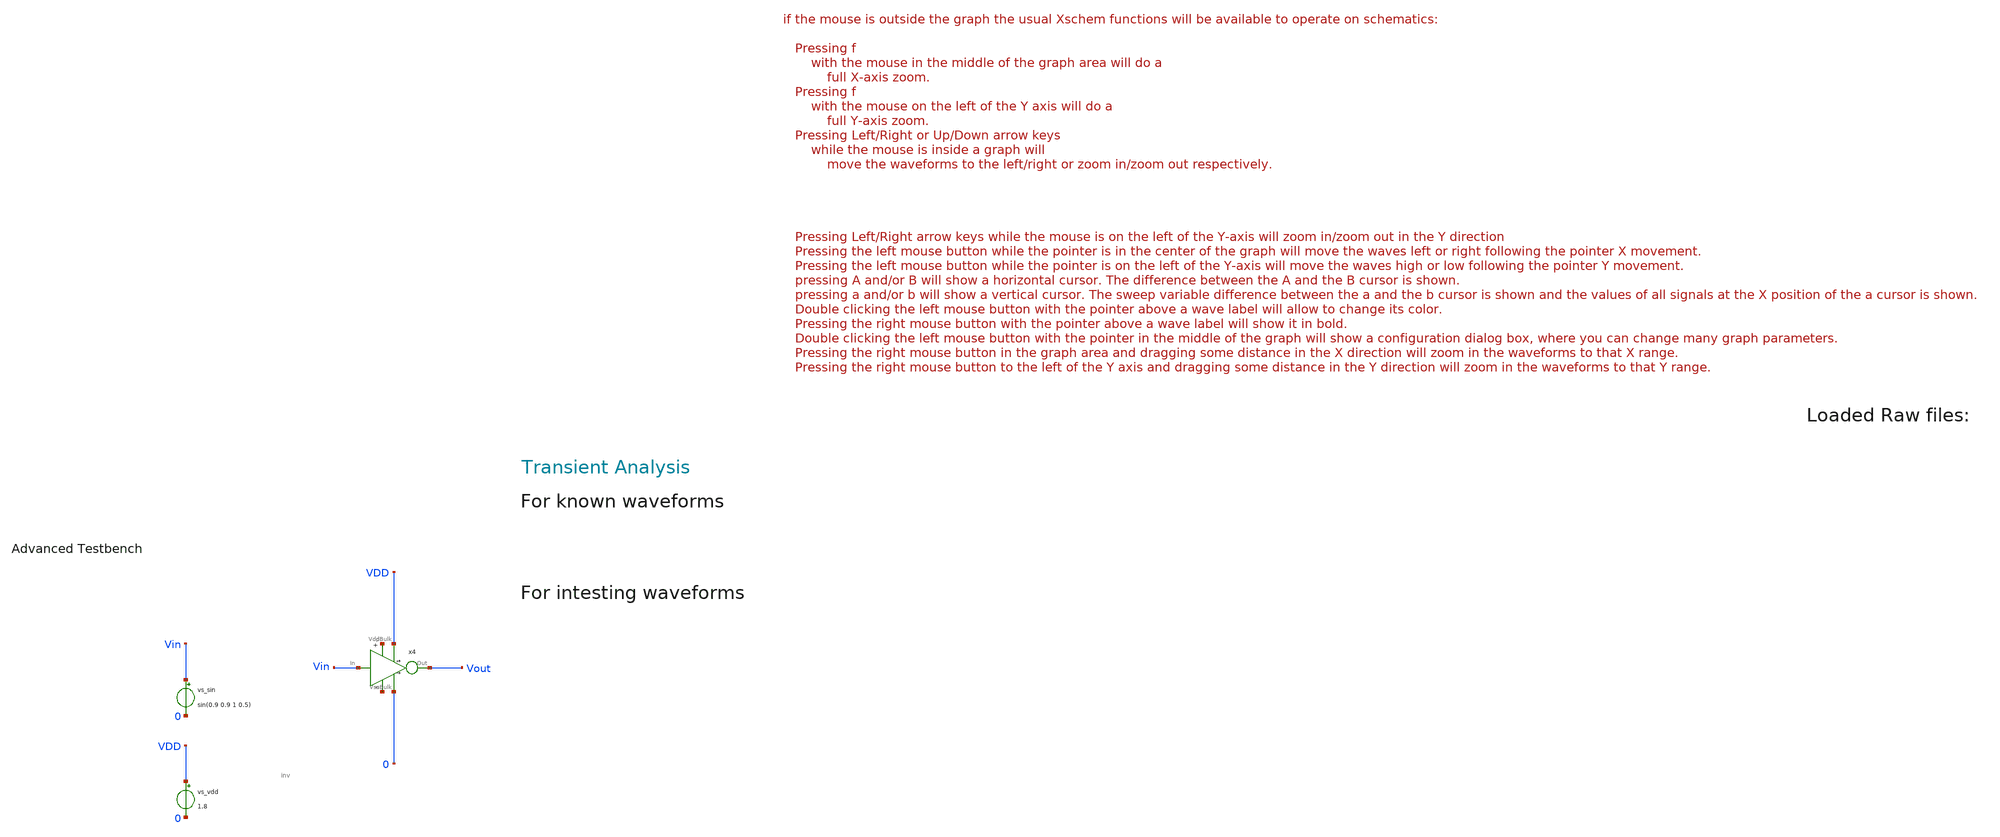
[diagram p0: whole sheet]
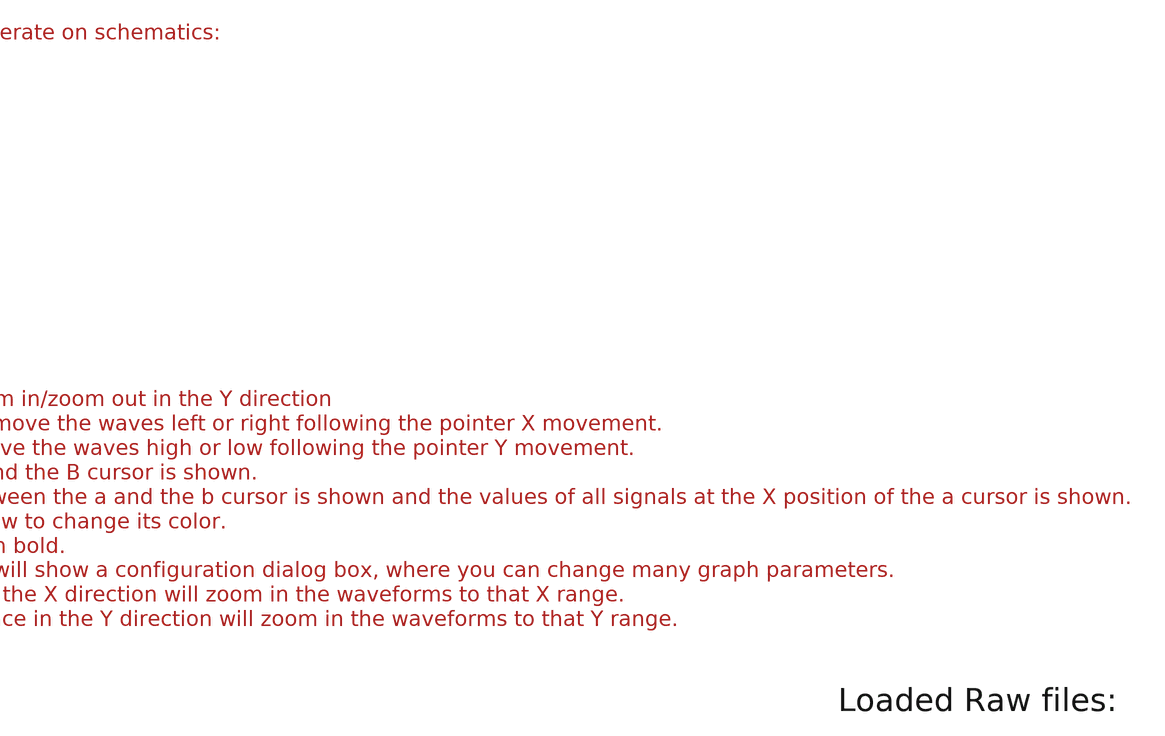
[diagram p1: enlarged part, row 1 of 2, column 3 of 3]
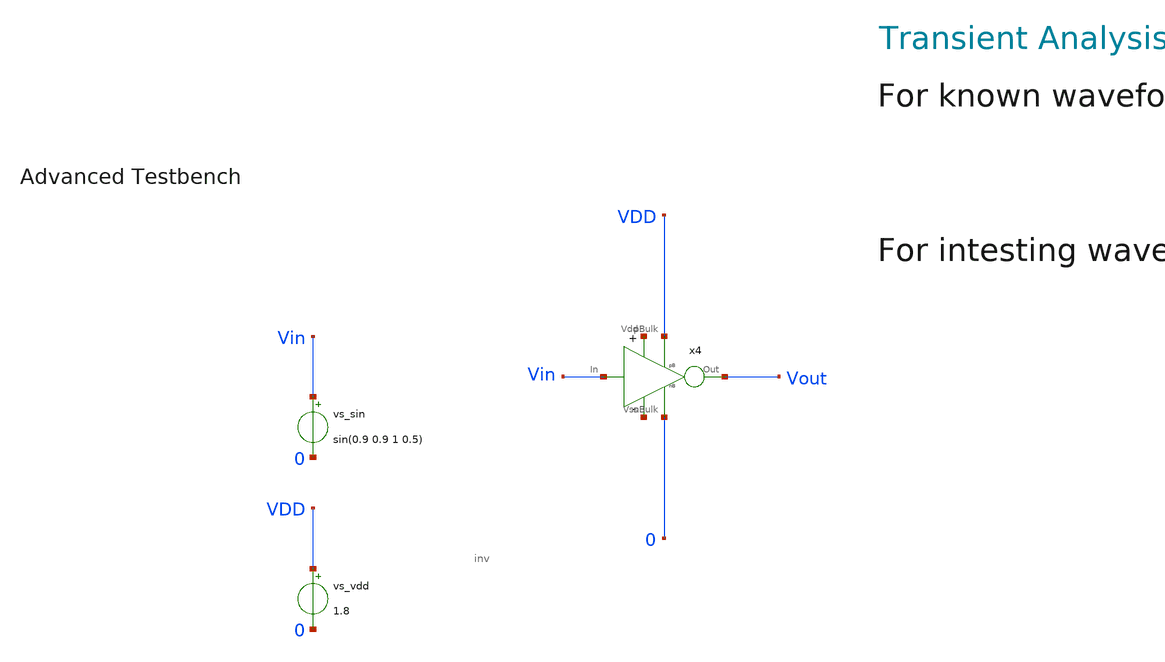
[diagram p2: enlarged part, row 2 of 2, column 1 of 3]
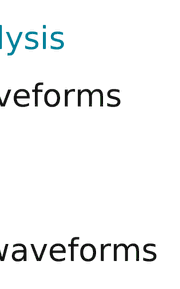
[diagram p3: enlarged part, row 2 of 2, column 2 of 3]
** sch_path: tt10-hdl/tt_um_test_commit/xschem/T0/inv/inv_Tran_tb.sch
* Copyright (C) 1998-2024 Stefan Frederik Schippers
* This program is free software; you can redistribute it and/or modify
* it under the terms of the GNU General Public License as published by
* the Free Software Foundation; either version 2 of the License, or
* (at your option) any later version.
* This program is distributed in the hope that it will be useful,
* but WITHOUT ANY WARRANTY; without even the implied warranty of
* MERCHANTABILITY or FITNESS FOR A PARTICULAR PURPOSE.  See the
* GNU General Public License for more details.
* You should have received a copy of the GNU General Public License
* along with this program; if not, write to the Free Software
**.subckt inv_Tran_tb
vs_vdd VDD 0 1.8
vs_sin Vin 0 sin(0.9 0.9 1 0.5)
x4 net1 net2 Vout Vin 0 VDD inv
**** begin user architecture code



.temp 30
*.param Vdd = 1.8
.option savecurrents
.save all *@m1[gm]
.control
  save all alli
  op
  remzerovec
  write schmTriggTran.raw
  set appendwrite

  tran 1m 2
  remzerovec
  write schmTriggTran.raw




  *quit 0




.endc





** opencircuitdesign pdks install
.lib $::SKYWATER_MODELS/sky130.lib.spice tt
.include $::SKYWATER_STDCELLS/sky130_fd_sc_hd.spice


**** end user architecture code
**.ends

* expanding   symbol:  T0/inv/inv.sym # of pins=6
** sym_path: tt10-hdl/tt_um_test_commit/xschem/T0/inv/inv.sym
** sch_path: tt10-hdl/tt_um_test_commit/xschem/T0/inv/inv.sch
.subckt inv Vdd Vss Out In nBulk pBulk
*.ipin Vdd
*.ipin Vss
*.opin Out
*.ipin In
*.ipin nBulk
*.ipin pBulk
XM1 Out In Vss nBulk sky130_fd_pr__nfet_01v8 L=0.15 W=1 nf=1 ad='int((1 + 1)/2) * 1 / 1 * 0.29' as='int((1 + 2)/2) * 1 / 1 * 0.29'
+ pd='2*int((1 + 1)/2) * (1 / 1 + 0.29)' ps='2*int((1 + 2)/2) * (1 / 1 + 0.29)' nrd='0.29 / 1 ' nrs='0.29 / 1 '
+ sa=0 sb=0 sd=0 mult=1 m=1
XM2 Out In Vdd pBulk sky130_fd_pr__pfet_01v8 L=0.15 W=1 nf=1 ad='int((nf+1)/2) * W/nf * 0.29' as='int((nf+2)/2) * W/nf * 0.29'
+ pd='2*int((nf+1)/2) * (W/nf + 0.29)' ps='2*int((nf+2)/2) * (W/nf + 0.29)' nrd='0.29 / W' nrs='0.29 / W'
+ sa=0 sb=0 sd=0 mult=1 m=1
.ends

.end
